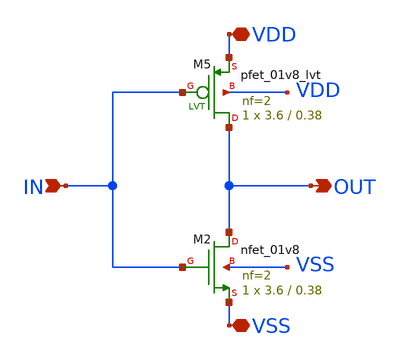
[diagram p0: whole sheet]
** sch_path: xschem/analog_inv.sch
**.subckt analog_inv VDD VSS IN OUT
*.iopin VDD
*.iopin VSS
*.ipin IN
*.opin OUT
XM2 OUT IN VSS VSS sky130_fd_pr__nfet_01v8 L=0.38 W=3.6 nf=2 ad='int((nf+1)/2) * W/nf * 0.29' as='int((nf+2)/2) * W/nf * 0.29'
+ pd='2*int((nf+1)/2) * (W/nf + 0.29)' ps='2*int((nf+2)/2) * (W/nf + 0.29)' nrd='0.29 / W' nrs='0.29 / W'
+ sa=0 sb=0 sd=0 mult=1 m=1
XM5 OUT IN VDD VDD sky130_fd_pr__pfet_01v8_lvt L=0.38 W=3.6 nf=2 ad='int((nf+1)/2) * W/nf * 0.29' as='int((nf+2)/2) * W/nf * 0.29'
+ pd='2*int((nf+1)/2) * (W/nf + 0.29)' ps='2*int((nf+2)/2) * (W/nf + 0.29)' nrd='0.29 / W' nrs='0.29 / W'
+ sa=0 sb=0 sd=0 mult=1 m=1
**.ends
.end
